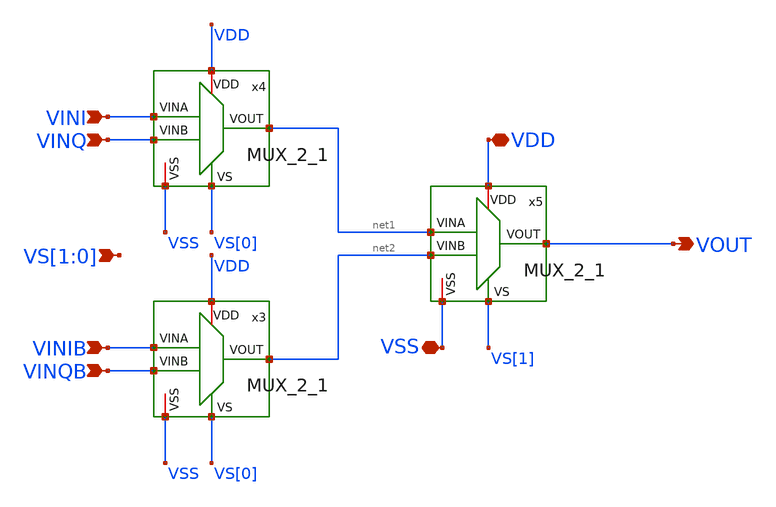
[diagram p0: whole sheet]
** sch_path: MUX_4_1.sch
**.subckt MUX_4_1 VOUT VDD VSS VINI VINQ VINIB VINQB VS[1],VS[0]
*.opin VOUT
*.iopin VDD
*.iopin VSS
*.ipin VINI
*.ipin VINQ
*.ipin VINIB
*.ipin VINQB
*.ipin VS[1],VS[0]
x3 VDD VINIB net2 VS[0] VINQB VSS MUX_2_1
x4 VDD VINI net1 VS[0] VINQ VSS MUX_2_1
x5 VDD net1 VOUT VS[1] net2 VSS MUX_2_1
**.ends
.end
